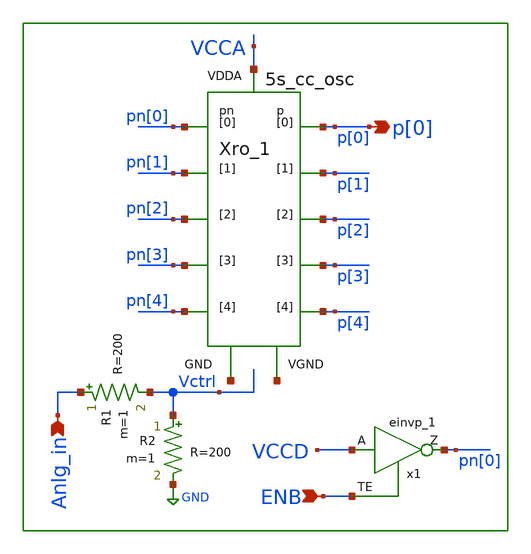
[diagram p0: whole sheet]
** sch_path: xschem/lib/ALib_VCO.sch
**.subckt ALib_VCO Anlg_in p[0] ENB
*.ipin Anlg_in
*.opin p[0]
*.ipin ENB
x1 VCCD ENB GND GND VCCD VCCD pn[0] sky130_fd_sc_hd__einvp_1
R2 Vctrl GND R=200 m=1
R1 Anlg_in Vctrl R=200 m=1
Xro_1 net1 VCCA p[0] p[1] p[2] p[3] p[4] pn[0] pn[1] pn[2] pn[3] pn[4] net2 5s_cc_osc
**.ends
.GLOBAL GND
.end
